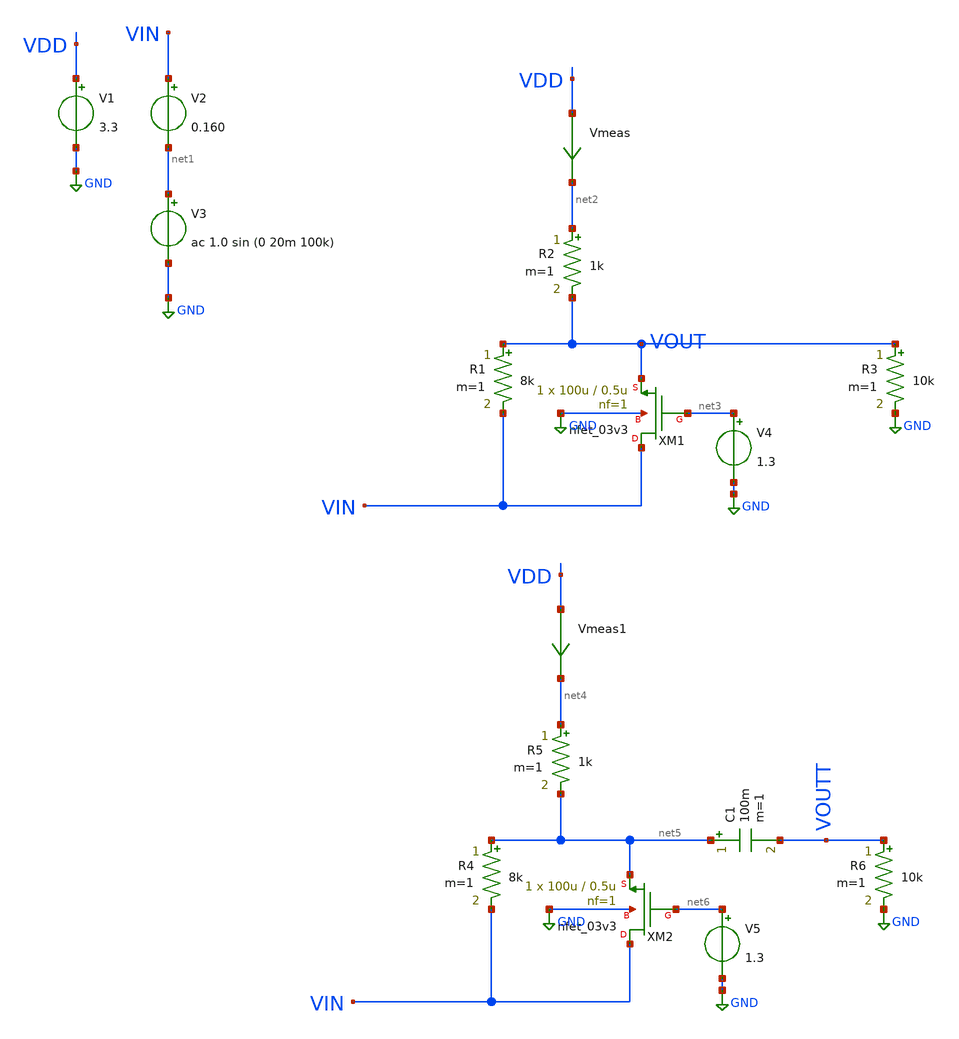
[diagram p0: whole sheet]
** sch_path: gain_with_load/simple_amp_with_load2.sch
**.subckt simple_amp_with_load2
Vmeas VDD net2 0
.save i(vmeas)
V1 VDD GND 3.3
V2 VIN net1 0.160
V3 net1 GND ac 1.0 sin (0 20m 100k)
R1 VOUT VIN 8k m=1
R2 net2 VOUT 1k m=1
XM1 VIN net3 VOUT GND nfet_03v3 L=0.5u W=100u nf=1 ad='int((nf+1)/2) * W/nf * 0.18u' as='int((nf+2)/2) * W/nf * 0.18u'
+ pd='2*int((nf+1)/2) * (W/nf + 0.18u)' ps='2*int((nf+2)/2) * (W/nf + 0.18u)' nrd='0.18u / W' nrs='0.18u / W'
+ sa=0 sb=0 sd=0 m=1
V4 net3 GND 1.3
R3 VOUT GND 10k m=1
Vmeas1 VDD net4 0
.save i(vmeas1)
R4 net5 VIN 8k m=1
R5 net4 net5 1k m=1
XM2 VIN net6 net5 GND nfet_03v3 L=0.5u W=100u nf=1 ad='int((nf+1)/2) * W/nf * 0.18u' as='int((nf+2)/2) * W/nf * 0.18u'
+ pd='2*int((nf+1)/2) * (W/nf + 0.18u)' ps='2*int((nf+2)/2) * (W/nf + 0.18u)' nrd='0.18u / W' nrs='0.18u / W'
+ sa=0 sb=0 sd=0 m=1
V5 net6 GND 1.3
R6 VOUTT GND 10k m=1
C1 net5 VOUTT 100m m=1
**** begin user architecture code

.include $::180MCU_MODELS/design.ngspice
*.lib $::180MCU_MODELS/sm141064.ngspice statistical
*.lib $::180MCU_MODELS/sm141064.ngspice res_statistical
.lib $::180MCU_MODELS/sm141064.ngspice typical
.lib $::180MCU_MODELS/sm141064.ngspice res_typical
.lib $::180MCU_MODELS/sm141064.ngspice moscap_typical
.lib $::180MCU_MODELS/sm141064.ngspice bjt_typical
.lib $::180MCU_MODELS/sm141064.ngspice diode_typical
.lib $::180MCU_MODELS/sm141064.ngspice mimcap_typical
.TEMP 27

.param   sw_stat_global = 1   sw_stat_mism = 1  mc_skew = 3  res_mc_skew = 3  cap_mc_skew = 3
+  fnoicor = 1



.control
save all
dc V2 0 3.3 0.01


plot v(VOUT) deriv(v(VOUT)) v(VIN)
plot v(VOUT) deriv(v(VOUT))
plot i(Vmeas)
plot deriv(v(VOUT))
tran 10ns 20u
plot (v(VOUTT)) (v(VIN)-0.160)
plot fft((v(VOUTT))) fft((v(VIN)))
ac dec 20 1 50G
plot v(VOUT)
.endc

**** end user architecture code
**.ends
.GLOBAL GND
.end
